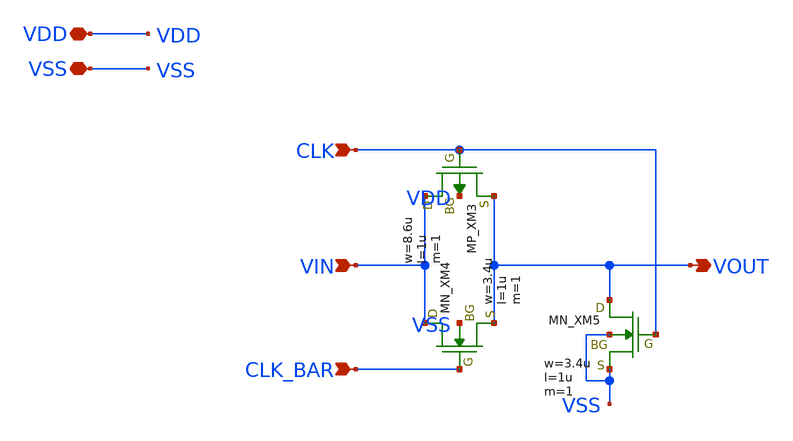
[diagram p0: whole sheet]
** sch_path: member_project/LPF/noritsuna/xschem/TG.sch
**.subckt TG VDD VSS CLK VIN VOUT CLK_BAR
*.iopin VDD
*.iopin VSS
*.ipin CLK
*.ipin VIN
*.opin VOUT
*.ipin CLK_BAR
XXM3 VIN CLK VOUT VDD PMOS w=8.6u l=1u nrd=0 nrs=0 m=1
XXM4 VIN CLK_BAR VOUT VSS NMOS w=3.4u l=1u nrd=0 nrs=0 m=1
XXM5 VOUT CLK VSS VSS NMOS w=3.4u l=1u nrd=0 nrs=0 m=1
**.ends
.end
